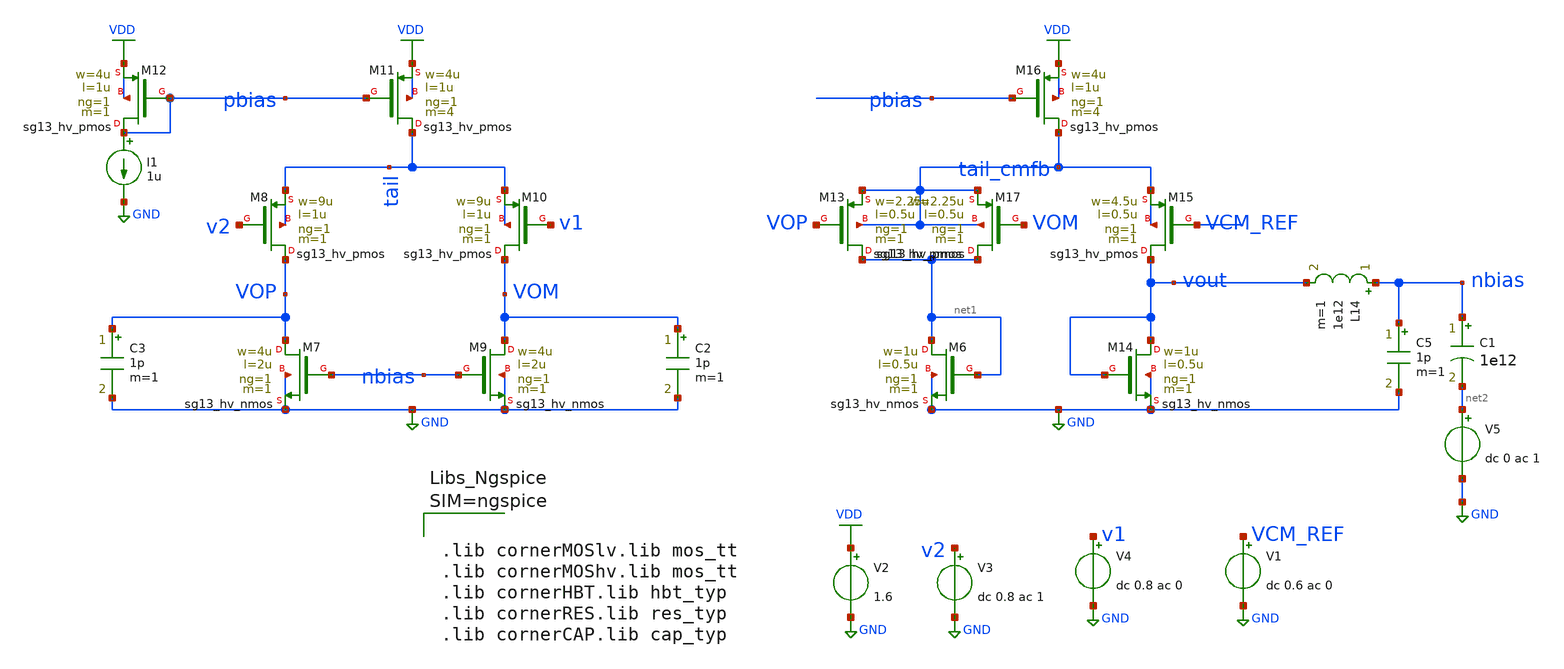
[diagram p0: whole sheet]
** sch_path: dependencies/OTA/OTA-main/schematic/xschem/Differntial_ended_stability_check.sch
**.subckt Differntial_ended_stability_check
V2 VDD GND 1.6
V3 v2 GND dc 0.8 ac 1
V4 v1 GND dc 0.8 ac 0
XM7 VOP nbias GND GND sg13_hv_nmos w=4u l=2u ng=1 m=1 mm_ok=1
XM8 VOP v2 tail tail sg13_hv_pmos w=9u l=1u ng=1 m=1 mm_ok=1
XM9 VOM nbias GND GND sg13_hv_nmos w=4u l=2u ng=1 m=1 mm_ok=1
XM10 VOM v1 tail tail sg13_hv_pmos w=9u l=1u ng=1 m=1 mm_ok=1
XM11 tail pbias VDD VDD sg13_hv_pmos w=4u l=1u ng=1 m=4 mm_ok=1
XM12 pbias pbias VDD VDD sg13_hv_pmos w=4u l=1u ng=1 m=1 mm_ok=1
I1 pbias GND 1u
C2 VOM GND 1p m=1
C3 VOP GND 1p m=1
XM6 net1 net1 GND GND sg13_hv_nmos w=1u l=0.5u ng=1 m=1 mm_ok=1
XM13 net1 VOP tail_cmfb tail_cmfb sg13_hv_pmos w=2.25u l=0.5u ng=1 m=1 mm_ok=1
XM14 vout vout GND GND sg13_hv_nmos w=1u l=0.5u ng=1 m=1 mm_ok=1
XM15 vout VCM_REF tail_cmfb tail_cmfb sg13_hv_pmos w=4.5u l=0.5u ng=1 m=1 mm_ok=1
XM16 tail_cmfb pbias VDD VDD sg13_hv_pmos w=4u l=1u ng=1 m=4 mm_ok=1
XM17 net1 VOM tail_cmfb tail_cmfb sg13_hv_pmos w=2.25u l=0.5u ng=1 m=1 mm_ok=1
V1 VCM_REF GND dc 0.6 ac 0
C1 nbias net2 1e12 m=1
V5 net2 GND dc 0 ac 1
L14 nbias vout 1e12 m=1
C5 nbias GND 1p m=1
**** begin user architecture code



.lib cornerMOSlv.lib mos_tt
.lib cornerMOShv.lib mos_tt
.lib cornerHBT.lib hbt_typ
.lib cornerRES.lib res_typ
.lib cornerCAP.lib cap_typ







.ac dec 10 100 10e8
*.save all
*.op



**** end user architecture code
**.ends
.GLOBAL GND
.GLOBAL VDD
.end
